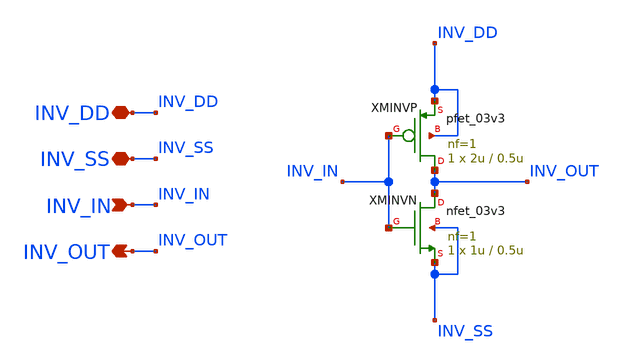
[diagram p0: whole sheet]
** sch_path: Design_Files/IC Design/Schematic/AFE_BLOCKS/INV/INV.sch
**.subckt INV INV_DD INV_SS INV_IN INV_OUT
*.iopin INV_DD
*.iopin INV_SS
*.ipin INV_IN
*.opin INV_OUT
XMINVP INV_OUT INV_IN INV_DD INV_DD pfet_03v3 L=0.5u W=2u nf=1 ad='int((nf+1)/2) * W/nf * 0.18u' as='int((nf+2)/2) * W/nf * 0.18u'
+ pd='2*int((nf+1)/2) * (W/nf + 0.18u)' ps='2*int((nf+2)/2) * (W/nf + 0.18u)' nrd='0.18u / W' nrs='0.18u / W'
+ sa=0 sb=0 sd=0 m=1
XMINVN INV_OUT INV_IN INV_SS INV_SS nfet_03v3 L=0.5u W=1u nf=1 ad='int((nf+1)/2) * W/nf * 0.18u' as='int((nf+2)/2) * W/nf * 0.18u'
+ pd='2*int((nf+1)/2) * (W/nf + 0.18u)' ps='2*int((nf+2)/2) * (W/nf + 0.18u)' nrd='0.18u / W' nrs='0.18u / W'
+ sa=0 sb=0 sd=0 m=1
**.ends
.end
